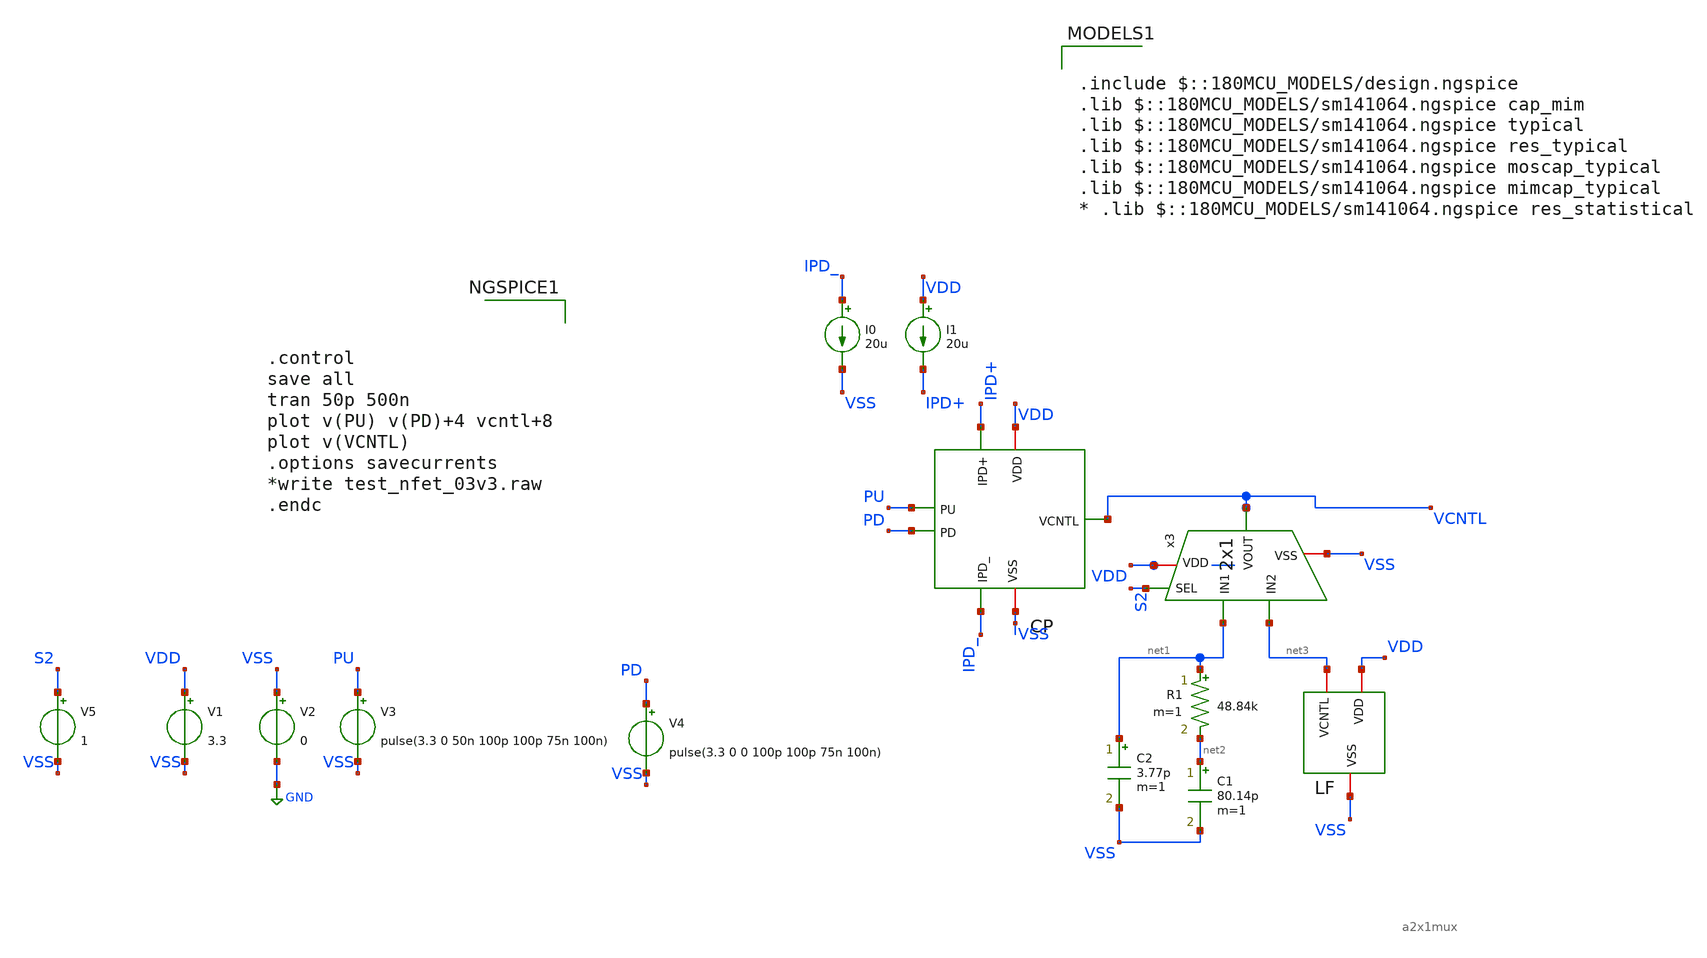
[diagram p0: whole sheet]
** sch_path: Clock_Generator_PAKISTAN_02/Schematics/untitled-4.sch
**.subckt untitled-4
V1 VDD VSS 3.3
V2 VSS GND 0
V3 PU VSS pulse(3.3 0 50n 100p 100p 75n 100n)
V4 PD VSS pulse(3.3 0 0 100p 100p 75n 100n)
x1 IPD+ IPD_ PU PD VCNTL VSS VDD CP
I0 IPD_ VSS 20u
I1 VDD IPD+ 20u
x2 net3 VDD VSS LF
C1 net2 VSS 80.14p m=1
C2 net1 VSS 3.77p m=1
R1 net1 net2 48.84k m=1
V5 S2 VSS 1
x3 net1 VDD VCNTL S2 VSS net3 a2x1mux
**** begin user architecture code



.control
save all
tran 50p 500n
plot v(PU) v(PD)+4 vcntl+8
plot v(VCNTL)
.options savecurrents
*write test_nfet_03v3.raw
.endc



.include $::180MCU_MODELS/design.ngspice
.lib $::180MCU_MODELS/sm141064.ngspice cap_mim
.lib $::180MCU_MODELS/sm141064.ngspice typical
.lib $::180MCU_MODELS/sm141064.ngspice res_typical
.lib $::180MCU_MODELS/sm141064.ngspice moscap_typical
.lib $::180MCU_MODELS/sm141064.ngspice mimcap_typical
* .lib $::180MCU_MODELS/sm141064.ngspice res_statistical

**** end user architecture code
**.ends
.GLOBAL GND
.end
